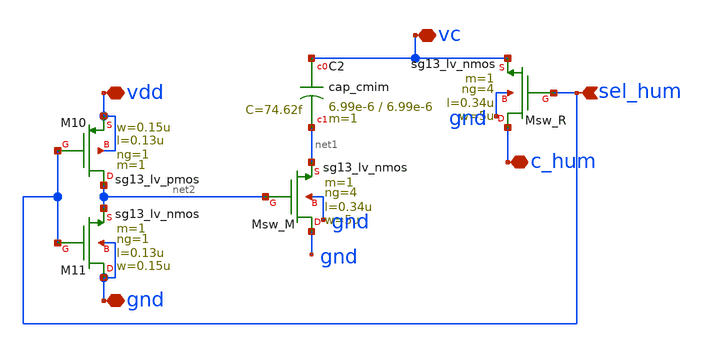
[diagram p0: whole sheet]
** sch_path: Enfoque_B/xschem/celdas/sel_c_hum.sch
**.subckt sel_c_hum c_hum vc sel_hum vdd gnd
*.iopin c_hum
*.iopin vc
*.ipin sel_hum
*.iopin vdd
*.iopin gnd
XMsw_R c_hum sel_hum vc gnd sg13_lv_nmos w=5u l=0.34u ng=4 m=1 mm_ok=1
XMsw_M gnd net2 net1 gnd sg13_lv_nmos w=5u l=0.34u ng=4 m=1 mm_ok=1
XM10 net2 sel_hum vdd vdd sg13_lv_pmos w=0.15u l=0.13u ng=1 m=1 mm_ok=1
XM11 gnd sel_hum net2 gnd sg13_lv_nmos w=0.15u l=0.13u ng=1 m=1 mm_ok=1
XC2 vc net1 cap_cmim w=6.99e-6 l=6.99e-6 m=1 mm_ok=1
**.ends
.end
